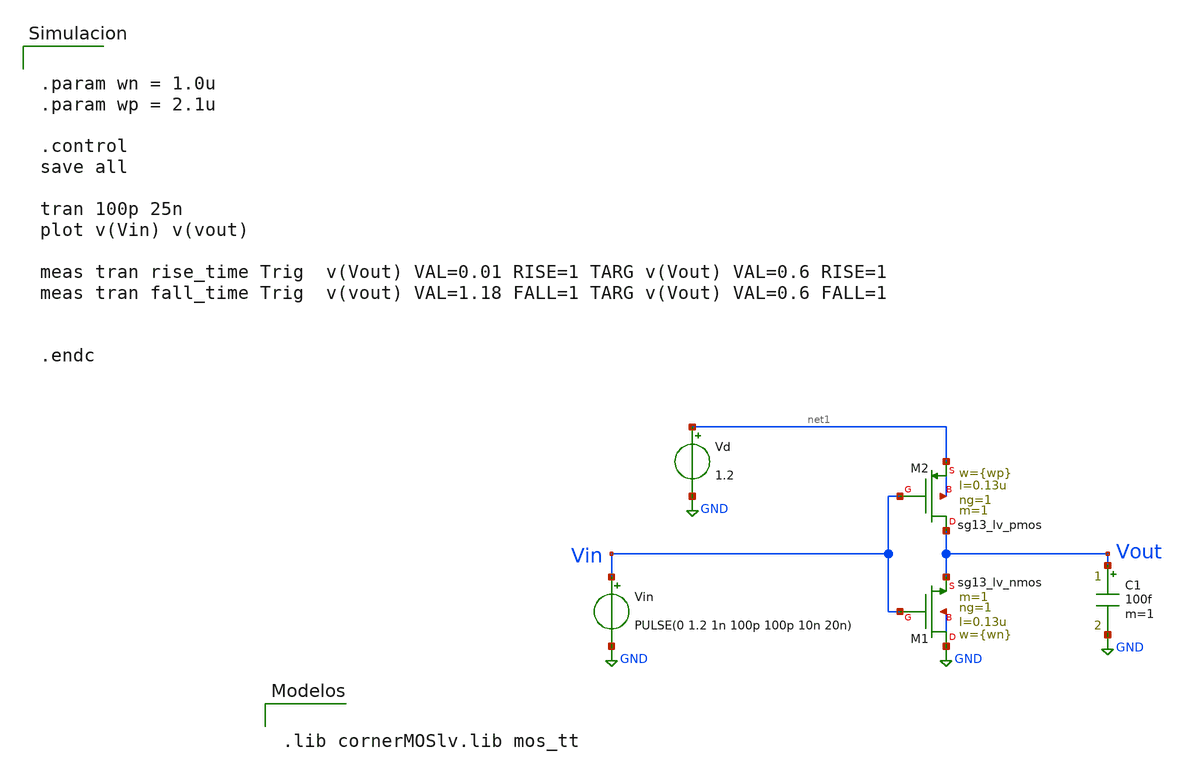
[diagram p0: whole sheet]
** sch_path: Taller2/Resuelto/inv_test_dimensionado.sch
**.subckt inv_test_dimensionado
XM1 GND Vin Vout GND sg13_lv_nmos w={wn} l=0.13u ng=1 m=1 mm_ok=1
XM2 Vout Vin net1 net1 sg13_lv_pmos w={wp} l=0.13u ng=1 m=1 mm_ok=1
Vin Vin GND PULSE(0 1.2 1n 100p 100p 10n 20n)
Vd net1 GND 1.2
C1 Vout GND 100f m=1
**** begin user architecture code


.lib cornerMOSlv.lib mos_tt




.param wn = 1.0u
.param wp = 2.1u

.control
save all

tran 100p 25n
plot v(Vin) v(vout)

meas tran rise_time Trig  v(Vout) VAL=0.01 RISE=1 TARG v(Vout) VAL=0.6 RISE=1
meas tran fall_time Trig  v(vout) VAL=1.18 FALL=1 TARG v(Vout) VAL=0.6 FALL=1


.endc


**** end user architecture code
**.ends
.GLOBAL GND
.end
